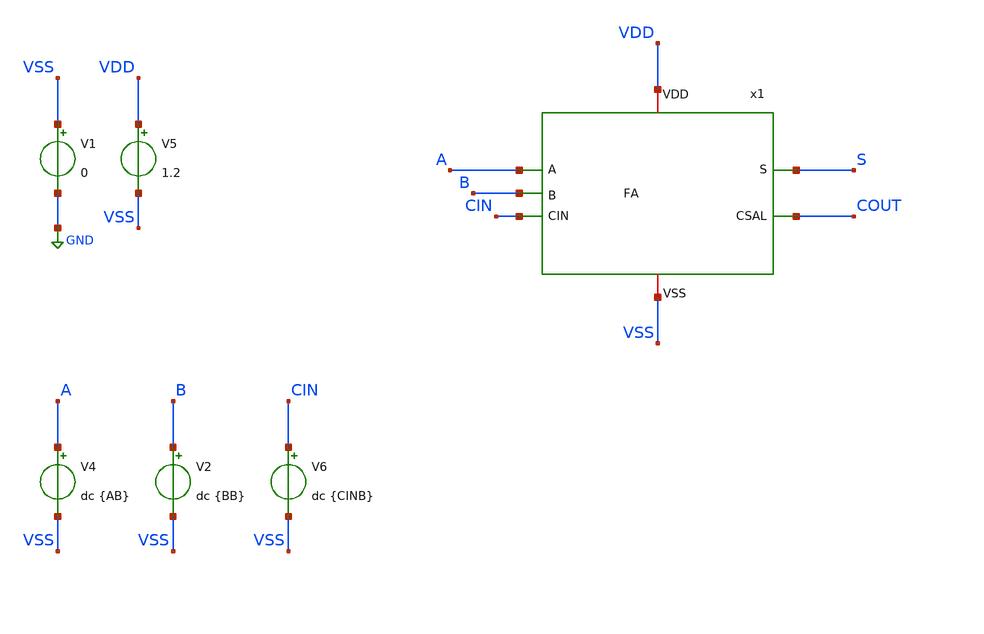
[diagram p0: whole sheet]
** sch_path: ADC8711-main/testbenches/tran/xschem/tb_FA.sch
**.subckt tb_FA
V1 VSS GND 0
V5 VDD VSS 1.2
V4 A VSS dc {AB}
V2 B VSS dc {BB}
V6 CIN VSS dc {CINB}
x1 A VDD B S VSS CIN COUT FA
**** begin user architecture code


.param temp=65
.param AB=1
.param BB=0
.param CINB=0

.control
save all
tran 0.5n 100n
write counter2_tb.raw
set appendwrite
.endc




.lib cornerMOSlv.lib mos_tt

**** end user architecture code
**.ends
.GLOBAL GND
.end
